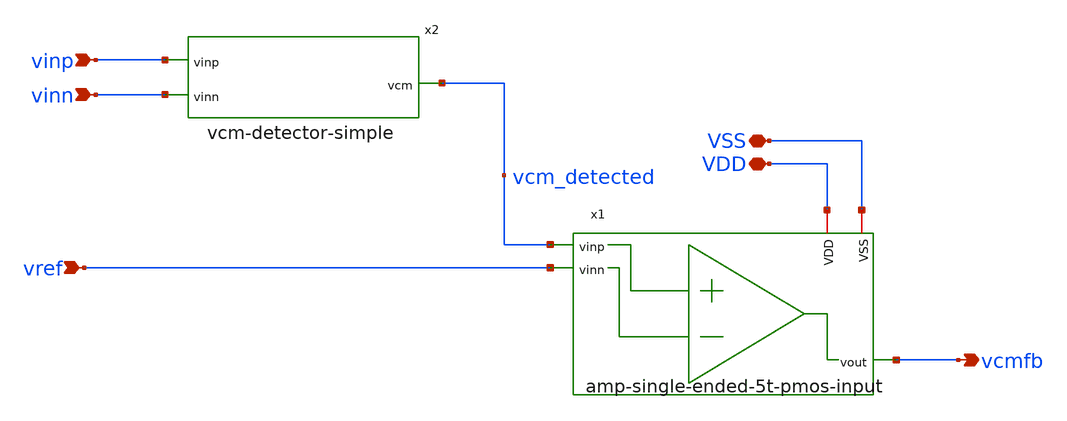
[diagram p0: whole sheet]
** sch_path: analog-db/circuits/cmfb_002_5t_pmos_input/pdk/ihp-sg13g2/schematic/cmfb-output-amp-5t-pmos-input.sch
* Copyright 2026 MacAnalog Research Group
**.subckt cmfb-output-amp-5t-pmos-input VSS VDD vinp vinn vcmfb vref
*.iopin VSS
*.iopin VDD
*.ipin vinp
*.ipin vinn
*.opin vcmfb
*.ipin vref
x2 vcm_detected vinp vinn vcm-detector-simple
x1 vcmfb vcm_detected vref VSS VDD amp-single-ended-5t-pmos-input
**.ends
.end
